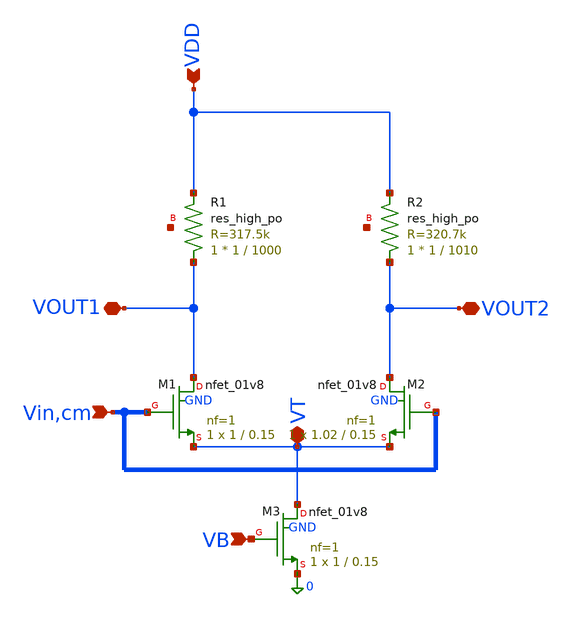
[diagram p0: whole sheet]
** sch_path: MOS-Circuits/Differential Pair/Diff_pair_3/diff_pair_mismatch.sch
**.subckt diff_pair_mismatch Vin,cm VDD VB VOUT2 VOUT1 VT
*.ipin Vin,cm
*.ipin VDD
*.ipin VB
*.iopin VOUT2
*.iopin VOUT1
*.iopin VT
XM1 VOUT1 Vin VT GND sky130_fd_pr__nfet_01v8 L=0.15 W=1 nf=1 ad='int((nf+1)/2) * W/nf * 0.29' as='int((nf+2)/2) * W/nf * 0.29'
+ pd='2*int((nf+1)/2) * (W/nf + 0.29)' ps='2*int((nf+2)/2) * (W/nf + 0.29)' nrd='0.29 / W' nrs='0.29 / W'
+ sa=0 sb=0 sd=0 mult=1 m=1
XM2 VOUT2 Vin VT GND sky130_fd_pr__nfet_01v8 L=0.15 W=1.02 nf=1 ad='int((nf+1)/2) * W/nf * 0.29' as='int((nf+2)/2) * W/nf * 0.29'
+ pd='2*int((nf+1)/2) * (W/nf + 0.29)' ps='2*int((nf+2)/2) * (W/nf + 0.29)' nrd='0.29 / W' nrs='0.29 / W'
+ sa=0 sb=0 sd=0 mult=1 m=1
XM3 VT VB 0 GND sky130_fd_pr__nfet_01v8 L=0.15 W=1 nf=1 ad='int((nf+1)/2) * W/nf * 0.29' as='int((nf+2)/2) * W/nf * 0.29'
+ pd='2*int((nf+1)/2) * (W/nf + 0.29)' ps='2*int((nf+2)/2) * (W/nf + 0.29)' nrd='0.29 / W' nrs='0.29 / W'
+ sa=0 sb=0 sd=0 mult=1 m=1
XR1 VOUT1 VDD net1 sky130_fd_pr__res_high_po W=1 L=1000 mult=1 m=1
XR2 VOUT2 VDD net2 sky130_fd_pr__res_high_po W=1 L=1010 mult=1 m=1
**.ends
.end
